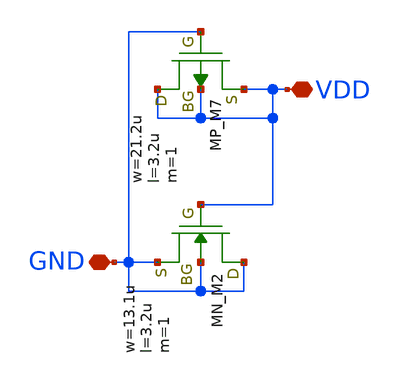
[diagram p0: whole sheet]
** sch_path: LEF/FILL2.sch
**.subckt FILL2 GND VDD
*.iopin GND
*.iopin VDD
XM7 VDD GND VDD VDD PMOS w=21.2u l=3.2u as=0 ad=0 ps=0 pd=0 nrd=0 nrs=0 m=1
XM2 GND VDD GND GND NMOS w=13.1u l=3.2u as=0 ad=0 ps=0 pd=0 nrd=0 nrs=0 m=1
**.ends
.end
